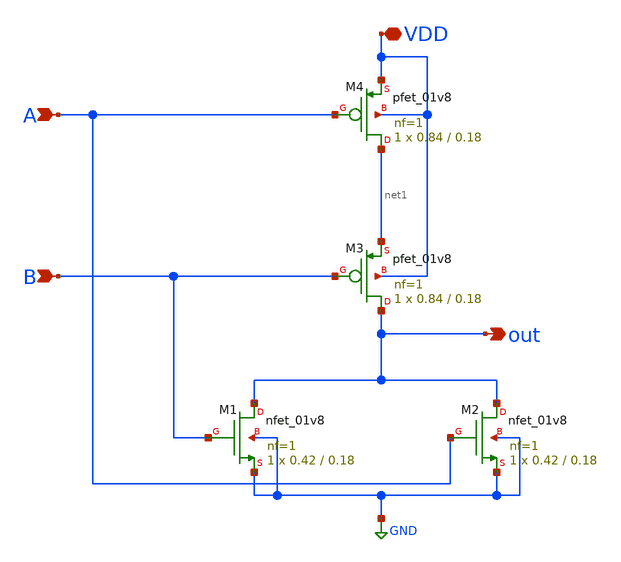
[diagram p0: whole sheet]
** sch_path: xschem/nor.sch
**.subckt nor VDD A B out
*.iopin VDD
*.ipin A
*.ipin B
*.opin out
XM1 out B GND GND sky130_fd_pr__nfet_01v8 L=0.18 W=0.42 nf=1 ad='int((nf+1)/2) * W/nf * 0.29' as='int((nf+2)/2) * W/nf * 0.29'
+ pd='2*int((nf+1)/2) * (W/nf + 0.29)' ps='2*int((nf+2)/2) * (W/nf + 0.29)' nrd='0.29 / W' nrs='0.29 / W'
+ sa=0 sb=0 sd=0 mult=1 m=1
XM2 out A GND GND sky130_fd_pr__nfet_01v8 L=0.18 W=0.42 nf=1 ad='int((nf+1)/2) * W/nf * 0.29' as='int((nf+2)/2) * W/nf * 0.29'
+ pd='2*int((nf+1)/2) * (W/nf + 0.29)' ps='2*int((nf+2)/2) * (W/nf + 0.29)' nrd='0.29 / W' nrs='0.29 / W'
+ sa=0 sb=0 sd=0 mult=1 m=1
XM3 out B net1 VDD sky130_fd_pr__pfet_01v8 L=0.18 W=0.84 nf=1 ad='int((nf+1)/2) * W/nf * 0.29' as='int((nf+2)/2) * W/nf * 0.29'
+ pd='2*int((nf+1)/2) * (W/nf + 0.29)' ps='2*int((nf+2)/2) * (W/nf + 0.29)' nrd='0.29 / W' nrs='0.29 / W'
+ sa=0 sb=0 sd=0 mult=1 m=1
XM4 net1 A VDD VDD sky130_fd_pr__pfet_01v8 L=0.18 W=0.84 nf=1 ad='int((nf+1)/2) * W/nf * 0.29' as='int((nf+2)/2) * W/nf * 0.29'
+ pd='2*int((nf+1)/2) * (W/nf + 0.29)' ps='2*int((nf+2)/2) * (W/nf + 0.29)' nrd='0.29 / W' nrs='0.29 / W'
+ sa=0 sb=0 sd=0 mult=1 m=1
**.ends
.GLOBAL GND
.end
